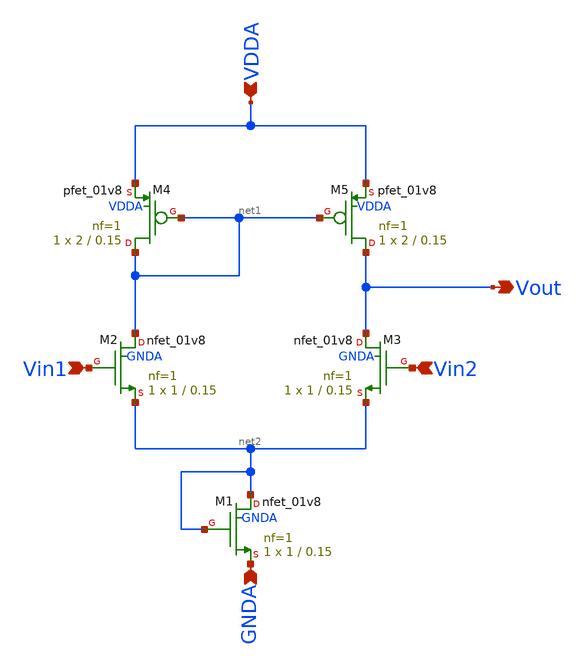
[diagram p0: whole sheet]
** sch_path: projects/pll/bandgapref/xschem_ngspice/opamp_bandgap.sch
**.subckt opamp_bandgap Vin1 Vout Vin2 GNDA VDDA
*.ipin Vin1
*.opin Vout
*.ipin Vin2
*.ipin GNDA
*.ipin VDDA
XM2 net1 Vin1 net2 GNDA sky130_fd_pr__nfet_01v8 L=0.15 W=1 nf=1 ad='int((nf+1)/2) * W/nf * 0.29' as='int((nf+2)/2) * W/nf * 0.29'
+ pd='2*int((nf+1)/2) * (W/nf + 0.29)' ps='2*int((nf+2)/2) * (W/nf + 0.29)' nrd='0.29 / W' nrs='0.29 / W'
+ sa=0 sb=0 sd=0 mult=1 m=1
XM3 Vout Vin2 net2 GNDA sky130_fd_pr__nfet_01v8 L=0.15 W=1 nf=1 ad='int((nf+1)/2) * W/nf * 0.29' as='int((nf+2)/2) * W/nf * 0.29'
+ pd='2*int((nf+1)/2) * (W/nf + 0.29)' ps='2*int((nf+2)/2) * (W/nf + 0.29)' nrd='0.29 / W' nrs='0.29 / W'
+ sa=0 sb=0 sd=0 mult=1 m=1
XM4 net1 net1 VDDA VDDA sky130_fd_pr__pfet_01v8 L=0.15 W=2 nf=1 ad='int((nf+1)/2) * W/nf * 0.29' as='int((nf+2)/2) * W/nf * 0.29'
+ pd='2*int((nf+1)/2) * (W/nf + 0.29)' ps='2*int((nf+2)/2) * (W/nf + 0.29)' nrd='0.29 / W' nrs='0.29 / W'
+ sa=0 sb=0 sd=0 mult=1 m=1
XM5 Vout net1 VDDA VDDA sky130_fd_pr__pfet_01v8 L=0.15 W=2 nf=1 ad='int((nf+1)/2) * W/nf * 0.29' as='int((nf+2)/2) * W/nf * 0.29'
+ pd='2*int((nf+1)/2) * (W/nf + 0.29)' ps='2*int((nf+2)/2) * (W/nf + 0.29)' nrd='0.29 / W' nrs='0.29 / W'
+ sa=0 sb=0 sd=0 mult=1 m=1
XM1 net2 net2 GNDA GNDA sky130_fd_pr__nfet_01v8 L=0.15 W=1 nf=1 ad='int((nf+1)/2) * W/nf * 0.29' as='int((nf+2)/2) * W/nf * 0.29'
+ pd='2*int((nf+1)/2) * (W/nf + 0.29)' ps='2*int((nf+2)/2) * (W/nf + 0.29)' nrd='0.29 / W' nrs='0.29 / W'
+ sa=0 sb=0 sd=0 mult=1 m=1
**.ends
.end
